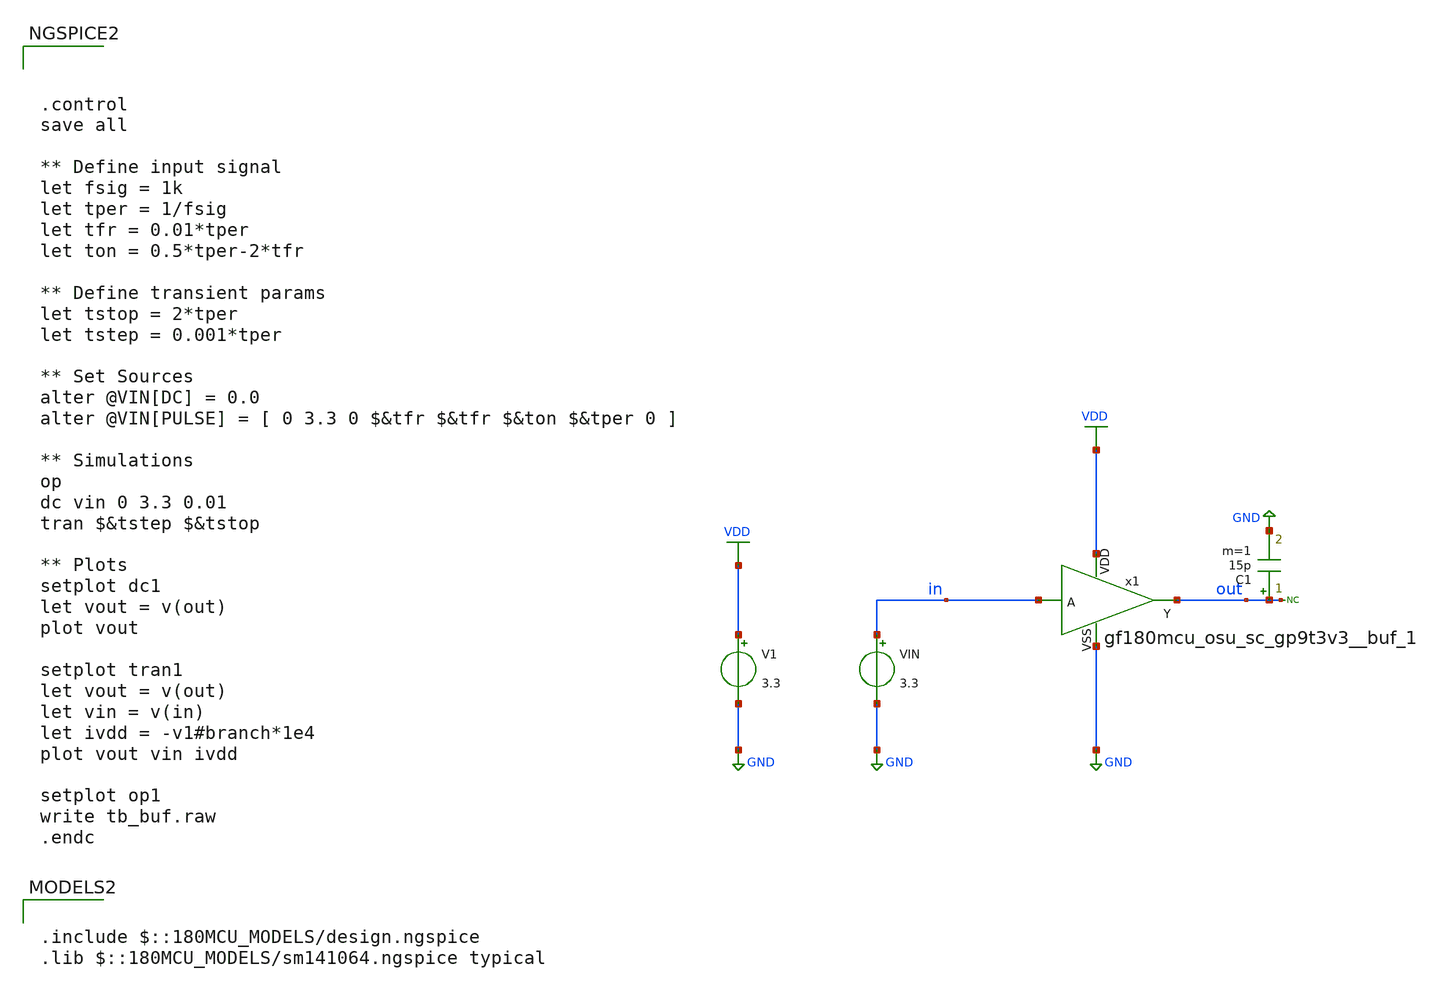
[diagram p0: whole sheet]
** sch_path: designs/comparator/final_magic/buffer/tb_buf.sch
**.subckt tb_buf
V1 VDD GND 3.3
VIN in GND 3.3
* noconn out
x1 in out VDD GND gf180mcu_osu_sc_gp9t3v3__buf_1
C1 out GND 15p m=1
**** begin user architecture code

.include $::180MCU_MODELS/design.ngspice
.lib $::180MCU_MODELS/sm141064.ngspice typical




.control
save all

** Define input signal
let fsig = 1k
let tper = 1/fsig
let tfr = 0.01*tper
let ton = 0.5*tper-2*tfr

** Define transient params
let tstop = 2*tper
let tstep = 0.001*tper

** Set Sources
alter @VIN[DC] = 0.0
alter @VIN[PULSE] = [ 0 3.3 0 $&tfr $&tfr $&ton $&tper 0 ]

** Simulations
op
dc vin 0 3.3 0.01
tran $&tstep $&tstop

** Plots
setplot dc1
let vout = v(out)
plot vout

setplot tran1
let vout = v(out)
let vin = v(in)
let ivdd = -v1#branch*1e4
plot vout vin ivdd

setplot op1
write tb_buf.raw
.endc


**** end user architecture code
**.ends
.GLOBAL VDD
.GLOBAL GND
.end
